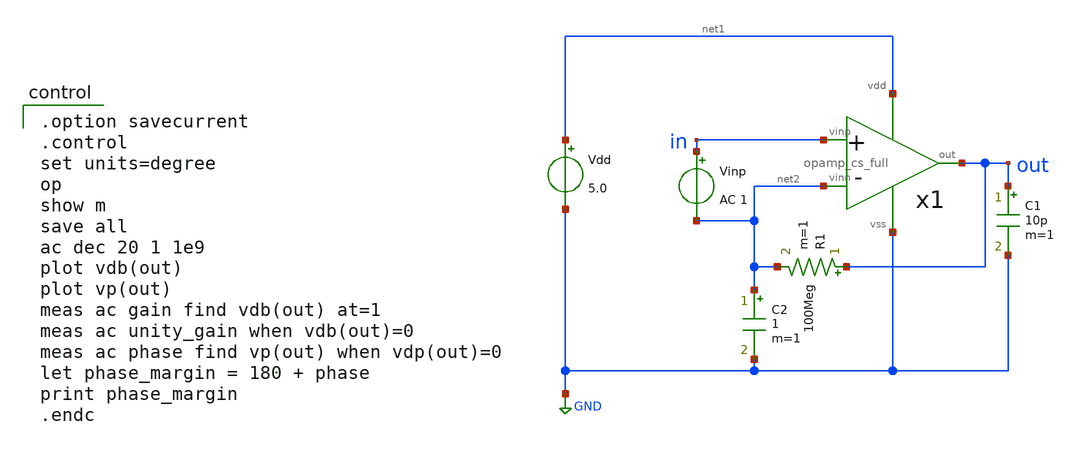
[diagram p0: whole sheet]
** sch_path: member_project/GroupWork/Team_Ando/dokunira/sch/opamp_cs_full_ac.sch
**.subckt opamp_cs_full_ac
Vdd net1 GND 5.0
Vinp in net2 AC 1
C1 out GND 10p m=1
R1 out net2 100Meg m=1
C2 net2 GND 1 m=1
x1 in net2 out net1 GND opamp_cs_full
**** begin user architecture code

.option savecurrent
.control
set units=degree
op
show m
save all
ac dec 20 1 1e9
plot vdb(out)
plot vp(out)
meas ac gain find vdb(out) at=1
meas ac unity_gain when vdb(out)=0
meas ac phase find vp(out) when vdp(out)=0
let phase_margin = 180 + phase
print phase_margin
.endc

 .include $::LIB/mos.lib
.include $::LIB/passive.lib
.include $::LIB/diode.lib
**** end user architecture code
**.ends

* expanding   symbol:  opamp_cs_full.sym # of pins=5
** sym_path: member_project/GroupWork/Team_Ando/dokunira/sch/opamp_cs_full.sym
** sch_path: member_project/GroupWork/Team_Ando/dokunira/sch/opamp_cs_full.sch
.subckt opamp_cs_full vinp vinn out vdd vss
*.iopin vdd
*.iopin vss
*.ipin vinn
*.ipin vinp
*.opin out
M12 net9 net1 net6 vss nmos L=1.6u W=16u m=1
M9 net1 net3 vdd vdd pmos L=1.6u W=32u m=1
M10 net1 net1 net2 vss nmos L=1.6u W=16u m=1
M11 net2 net2 vss vss nmos L=1.6u W=16u m=1
R1 vss net4 HR_poly W=2.0 L=20
M8 net3 net3 vdd vdd pmos L=1.6u W=32u m=1
M13 net5 net3 vdd vdd pmos L=1.6u W=32u m=1
M15 net3 net5 net4 vss nmos L=1.6u W=16u m=1
M14 net5 net4 vss vss nmos L=1.6u W=16u m=1
M5 net8 net3 vdd vdd pmos L=1.6u W=64u m=1
M1 net7 vinn net8 net8 pmos L=1.6u W=128u m=1
M2 net6 vinp net8 net8 pmos L=1.6u W=128u m=1
M3 net7 net7 vss vss nmos L=1.6u W=16u m=1
M4 net6 net7 vss vss nmos L=1.6u W=16u m=1
M6 out net3 vdd vdd pmos L=1.6u W=256u m=1
M7 out net6 vss vss nmos L=1.6u W=128u m=1
C1 out net9 Poly_cap W=20 L=22
.ends

.GLOBAL GND
.end
